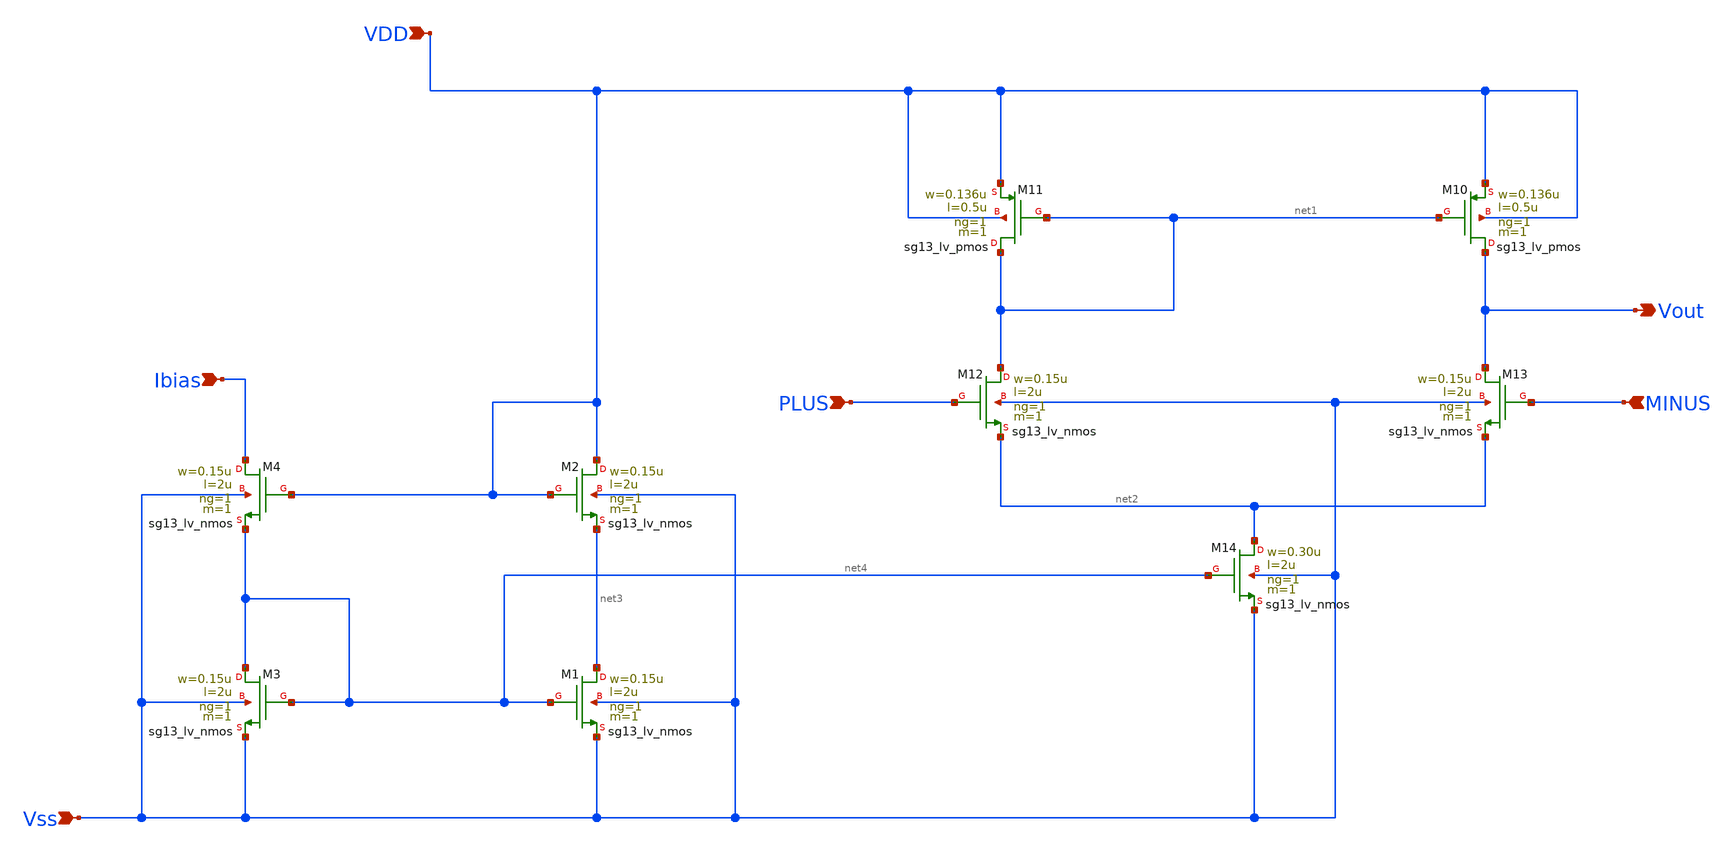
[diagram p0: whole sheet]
** sch_path: DSM/Schematics/Designs_Hrishi/RealCircuits/5-T_OTA/5-T_OTA.sch
* (c) 2024 Hrishikesh, @HSB
**.subckt 5-T_OTA MINUS PLUS VDD Ibias Vss Vout
*.ipin MINUS
*.ipin PLUS
*.ipin VDD
*.ipin Ibias
*.ipin Vss
*.opin Vout
XM10 Vout net1 VDD VDD sg13_lv_pmos w=0.136u l=0.5u ng=1 m=1 mm_ok=1
XM11 net1 net1 VDD VDD sg13_lv_pmos w=0.136u l=0.5u ng=1 m=1 mm_ok=1
XM12 net1 PLUS net2 Vss sg13_lv_nmos w=0.15u l=2u ng=1 m=1 mm_ok=1
XM13 Vout MINUS net2 Vss sg13_lv_nmos w=0.15u l=2u ng=1 m=1 mm_ok=1
XM14 net2 net4 Vss Vss sg13_lv_nmos w=0.30u l=2u ng=1 m=1 mm_ok=1
XM1 net3 net4 Vss Vss sg13_lv_nmos w=0.15u l=2u ng=1 m=1 mm_ok=1
XM2 VDD VDD net3 Vss sg13_lv_nmos w=0.15u l=2u ng=1 m=1 mm_ok=1
XM3 net4 net4 Vss Vss sg13_lv_nmos w=0.15u l=2u ng=1 m=1 mm_ok=1
XM4 Ibias VDD net4 Vss sg13_lv_nmos w=0.15u l=2u ng=1 m=1 mm_ok=1
**.ends
.end
